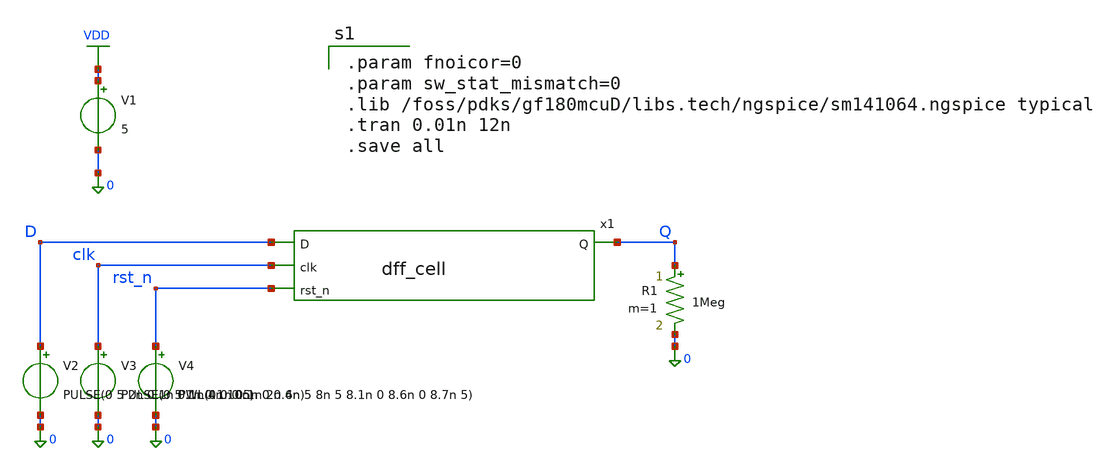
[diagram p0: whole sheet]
** sch_path: xschem/sar_adc/blocks/async_sar/testbench/tb_dff_cell.sch
**.subckt tb_dff_cell
V1 VDD 0 5
V2 D 0 PULSE(0 5 2n 0.1n 0.1n 4n 10n)
V3 clk 0 PULSE(0 5 1n 0.1n 0.1n 2n 4n)
V4 rst_n 0 PWL(0 0 0.5n 0 0.6n 5 8n 5 8.1n 0 8.6n 0 8.7n 5)
R1 Q 0 1Meg m=1
x1 D clk rst_n Q dff_cell
**** begin user architecture code

.param fnoicor=0
.param sw_stat_mismatch=0
.lib /foss/pdks/gf180mcuD/libs.tech/ngspice/sm141064.ngspice typical
.tran 0.01n 12n
.save all

**** end user architecture code
**.ends

* expanding   symbol:  sar_adc/blocks/async_sar/dff_cell.sym # of pins=4
** sym_path: xschem/sar_adc/dff_cell.sym
** sch_path: xschem/sar_adc/dff_cell.sch
.subckt dff_cell D clk rst_n Q
*.ipin clk
*.ipin D
*.ipin rst_n
*.opin Q
XM1 clk_n clk VDD VDD pfet_03v3 L=0.28u W=1.0u nf=1 ad='int((nf+1)/2) * W/nf * 0.18u' as='int((nf+2)/2) * W/nf * 0.18u'
+ pd='2*int((nf+1)/2) * (W/nf + 0.18u)' ps='2*int((nf+2)/2) * (W/nf + 0.18u)' nrd='0.18u / W' nrs='0.18u / W'
+ sa=0 sb=0 sd=0 m=1
XM2 clk_n clk 0 0 nfet_03v3 L=0.28u W=0.50u nf=1 ad='int((nf+1)/2) * W/nf * 0.18u' as='int((nf+2)/2) * W/nf * 0.18u'
+ pd='2*int((nf+1)/2) * (W/nf + 0.18u)' ps='2*int((nf+2)/2) * (W/nf + 0.18u)' nrd='0.18u / W' nrs='0.18u / W'
+ sa=0 sb=0 sd=0 m=1
XM3 M clk D_int VDD pfet_03v3 L=0.28u W=1.0u nf=1 ad='int((nf+1)/2) * W/nf * 0.18u' as='int((nf+2)/2) * W/nf * 0.18u'
+ pd='2*int((nf+1)/2) * (W/nf + 0.18u)' ps='2*int((nf+2)/2) * (W/nf + 0.18u)' nrd='0.18u / W' nrs='0.18u / W'
+ sa=0 sb=0 sd=0 m=1
XM4 D_int clk_n M 0 nfet_03v3 L=0.28u W=0.50u nf=1 ad='int((nf+1)/2) * W/nf * 0.18u' as='int((nf+2)/2) * W/nf * 0.18u'
+ pd='2*int((nf+1)/2) * (W/nf + 0.18u)' ps='2*int((nf+2)/2) * (W/nf + 0.18u)' nrd='0.18u / W' nrs='0.18u / W'
+ sa=0 sb=0 sd=0 m=1
XM5 M_bar M VDD VDD pfet_03v3 L=0.28u W=1.0u nf=1 ad='int((nf+1)/2) * W/nf * 0.18u' as='int((nf+2)/2) * W/nf * 0.18u'
+ pd='2*int((nf+1)/2) * (W/nf + 0.18u)' ps='2*int((nf+2)/2) * (W/nf + 0.18u)' nrd='0.18u / W' nrs='0.18u / W'
+ sa=0 sb=0 sd=0 m=1
XM6 M_bar M 0 0 nfet_03v3 L=0.28u W=0.50u nf=1 ad='int((nf+1)/2) * W/nf * 0.18u' as='int((nf+2)/2) * W/nf * 0.18u'
+ pd='2*int((nf+1)/2) * (W/nf + 0.18u)' ps='2*int((nf+2)/2) * (W/nf + 0.18u)' nrd='0.18u / W' nrs='0.18u / W'
+ sa=0 sb=0 sd=0 m=1
XM7 M M_bar VDD VDD pfet_03v3 L=2.0u W=0.30u nf=1 ad='int((nf+1)/2) * W/nf * 0.18u' as='int((nf+2)/2) * W/nf * 0.18u'
+ pd='2*int((nf+1)/2) * (W/nf + 0.18u)' ps='2*int((nf+2)/2) * (W/nf + 0.18u)' nrd='0.18u / W' nrs='0.18u / W'
+ sa=0 sb=0 sd=0 m=1
XM8 M M_bar 0 0 nfet_03v3 L=2.4u W=0.22u nf=1 ad='int((nf+1)/2) * W/nf * 0.18u' as='int((nf+2)/2) * W/nf * 0.18u'
+ pd='2*int((nf+1)/2) * (W/nf + 0.18u)' ps='2*int((nf+2)/2) * (W/nf + 0.18u)' nrd='0.18u / W' nrs='0.18u / W'
+ sa=0 sb=0 sd=0 m=1
XM9 S clk_n M_bar VDD pfet_03v3 L=0.28u W=1.0u nf=1 ad='int((nf+1)/2) * W/nf * 0.18u' as='int((nf+2)/2) * W/nf * 0.18u'
+ pd='2*int((nf+1)/2) * (W/nf + 0.18u)' ps='2*int((nf+2)/2) * (W/nf + 0.18u)' nrd='0.18u / W' nrs='0.18u / W'
+ sa=0 sb=0 sd=0 m=1
XM10 M_bar clk S 0 nfet_03v3 L=0.28u W=0.50u nf=1 ad='int((nf+1)/2) * W/nf * 0.18u' as='int((nf+2)/2) * W/nf * 0.18u'
+ pd='2*int((nf+1)/2) * (W/nf + 0.18u)' ps='2*int((nf+2)/2) * (W/nf + 0.18u)' nrd='0.18u / W' nrs='0.18u / W'
+ sa=0 sb=0 sd=0 m=1
XM11 Q_bar S VDD VDD pfet_03v3 L=0.28u W=1.0u nf=1 ad='int((nf+1)/2) * W/nf * 0.18u' as='int((nf+2)/2) * W/nf * 0.18u'
+ pd='2*int((nf+1)/2) * (W/nf + 0.18u)' ps='2*int((nf+2)/2) * (W/nf + 0.18u)' nrd='0.18u / W' nrs='0.18u / W'
+ sa=0 sb=0 sd=0 m=1
XM12 Q_bar rst_n VDD VDD pfet_03v3 L=0.28u W=1.0u nf=1 ad='int((nf+1)/2) * W/nf * 0.18u' as='int((nf+2)/2) * W/nf * 0.18u'
+ pd='2*int((nf+1)/2) * (W/nf + 0.18u)' ps='2*int((nf+2)/2) * (W/nf + 0.18u)' nrd='0.18u / W' nrs='0.18u / W'
+ sa=0 sb=0 sd=0 m=1
XM13 Q_bar S net1 0 nfet_03v3 L=0.28u W=0.50u nf=1 ad='int((nf+1)/2) * W/nf * 0.18u' as='int((nf+2)/2) * W/nf * 0.18u'
+ pd='2*int((nf+1)/2) * (W/nf + 0.18u)' ps='2*int((nf+2)/2) * (W/nf + 0.18u)' nrd='0.18u / W' nrs='0.18u / W'
+ sa=0 sb=0 sd=0 m=1
XM14 net1 rst_n 0 0 nfet_03v3 L=0.28u W=0.50u nf=1 ad='int((nf+1)/2) * W/nf * 0.18u' as='int((nf+2)/2) * W/nf * 0.18u'
+ pd='2*int((nf+1)/2) * (W/nf + 0.18u)' ps='2*int((nf+2)/2) * (W/nf + 0.18u)' nrd='0.18u / W' nrs='0.18u / W'
+ sa=0 sb=0 sd=0 m=1
XM15 Q Q_bar VDD VDD pfet_03v3 L=0.28u W=1.0u nf=1 ad='int((nf+1)/2) * W/nf * 0.18u' as='int((nf+2)/2) * W/nf * 0.18u'
+ pd='2*int((nf+1)/2) * (W/nf + 0.18u)' ps='2*int((nf+2)/2) * (W/nf + 0.18u)' nrd='0.18u / W' nrs='0.18u / W'
+ sa=0 sb=0 sd=0 m=1
XM16 Q Q_bar 0 0 nfet_03v3 L=0.28u W=0.50u nf=1 ad='int((nf+1)/2) * W/nf * 0.18u' as='int((nf+2)/2) * W/nf * 0.18u'
+ pd='2*int((nf+1)/2) * (W/nf + 0.18u)' ps='2*int((nf+2)/2) * (W/nf + 0.18u)' nrd='0.18u / W' nrs='0.18u / W'
+ sa=0 sb=0 sd=0 m=1
XM17 S Q_bar VDD VDD pfet_03v3 L=2.0u W=0.30u nf=1 ad='int((nf+1)/2) * W/nf * 0.18u' as='int((nf+2)/2) * W/nf * 0.18u'
+ pd='2*int((nf+1)/2) * (W/nf + 0.18u)' ps='2*int((nf+2)/2) * (W/nf + 0.18u)' nrd='0.18u / W' nrs='0.18u / W'
+ sa=0 sb=0 sd=0 m=1
XM18 S Q_bar 0 0 nfet_03v3 L=2.4u W=0.22u nf=1 ad='int((nf+1)/2) * W/nf * 0.18u' as='int((nf+2)/2) * W/nf * 0.18u'
+ pd='2*int((nf+1)/2) * (W/nf + 0.18u)' ps='2*int((nf+2)/2) * (W/nf + 0.18u)' nrd='0.18u / W' nrs='0.18u / W'
+ sa=0 sb=0 sd=0 m=1
XM19 D_int D VDD VDD pfet_03v3 L=0.28u W=1.0u nf=1 ad='int((nf+1)/2) * W/nf * 0.18u' as='int((nf+2)/2) * W/nf * 0.18u'
+ pd='2*int((nf+1)/2) * (W/nf + 0.18u)' ps='2*int((nf+2)/2) * (W/nf + 0.18u)' nrd='0.18u / W' nrs='0.18u / W'
+ sa=0 sb=0 sd=0 m=1
XM20 D_int D 0 0 nfet_03v3 L=0.28u W=0.50u nf=1 ad='int((nf+1)/2) * W/nf * 0.18u' as='int((nf+2)/2) * W/nf * 0.18u'
+ pd='2*int((nf+1)/2) * (W/nf + 0.18u)' ps='2*int((nf+2)/2) * (W/nf + 0.18u)' nrd='0.18u / W' nrs='0.18u / W'
+ sa=0 sb=0 sd=0 m=1
.ends

.GLOBAL VDD
.end
